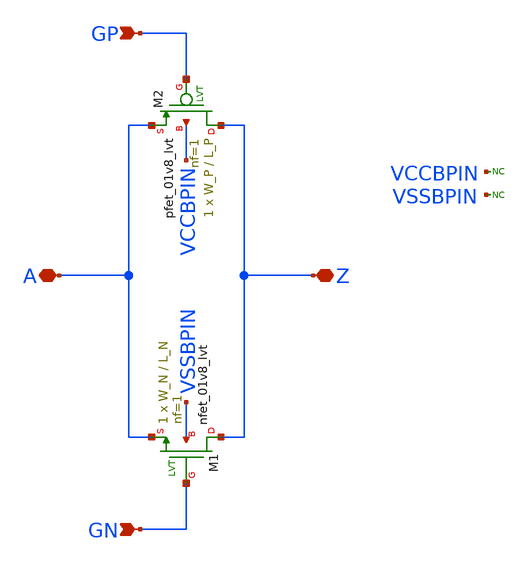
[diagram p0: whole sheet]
** sch_path: sky130A/xschem_libs/sky130_tests/passgate_nlvt/schematic/passgate_nlvt.sch
* Copyright 2021 Stefan Frederik Schippers
* Licensed under the Apache License, Version 2.0 (the "License");
* you may not use this file except in compliance with the License.
* You may obtain a copy of the License at
* https://www.apache.org/licenses/LICENSE-2.0
* Unless required by applicable law or agreed to in writing, software
* distributed under the License is distributed on an "AS IS" BASIS,
* WITHOUT WARRANTIES OR CONDITIONS OF ANY KIND, either express or implied.
* See the License for the specific language governing permissions and
* limitations under the License.
**.subckt passgate_nlvt A Z GP GN
*.iopin A
*.iopin Z
*.ipin GP
*.ipin GN
XM1 Z GN A VSSBPIN sky130_fd_pr__nfet_01v8_lvt L=L_N W=W_N nf=1 ad='int((1 + 1)/2) * W_N / 1 * 0.29'
+ as='int((1 + 2)/2) * W_N / 1 * 0.29' pd='2*int((1 + 1)/2) * (W_N / 1 + 0.29)' ps='2*int((1 + 2)/2) * (W_N / 1 + 0.29)'
+ nrd='0.29 / W_N ' nrs='0.29 / W_N ' sa=0 sb=0 sd=0 mult=1 m=1
XM2 Z GP A VCCBPIN sky130_fd_pr__pfet_01v8_lvt L=L_P W=W_P nf=1 ad='int((1 + 1)/2) * W_P / 1 * 0.29'
+ as='int((1 + 2)/2) * W_P / 1 * 0.29' pd='2*int((1 + 1)/2) * (W_P / 1 + 0.29)' ps='2*int((1 + 2)/2) * (W_P / 1 + 0.29)'
+ nrd='0.29 / W_P ' nrs='0.29 / W_P ' sa=0 sb=0 sd=0 mult=1 m=1
* noconn VCCBPIN
* noconn VSSBPIN
**.ends
.end
